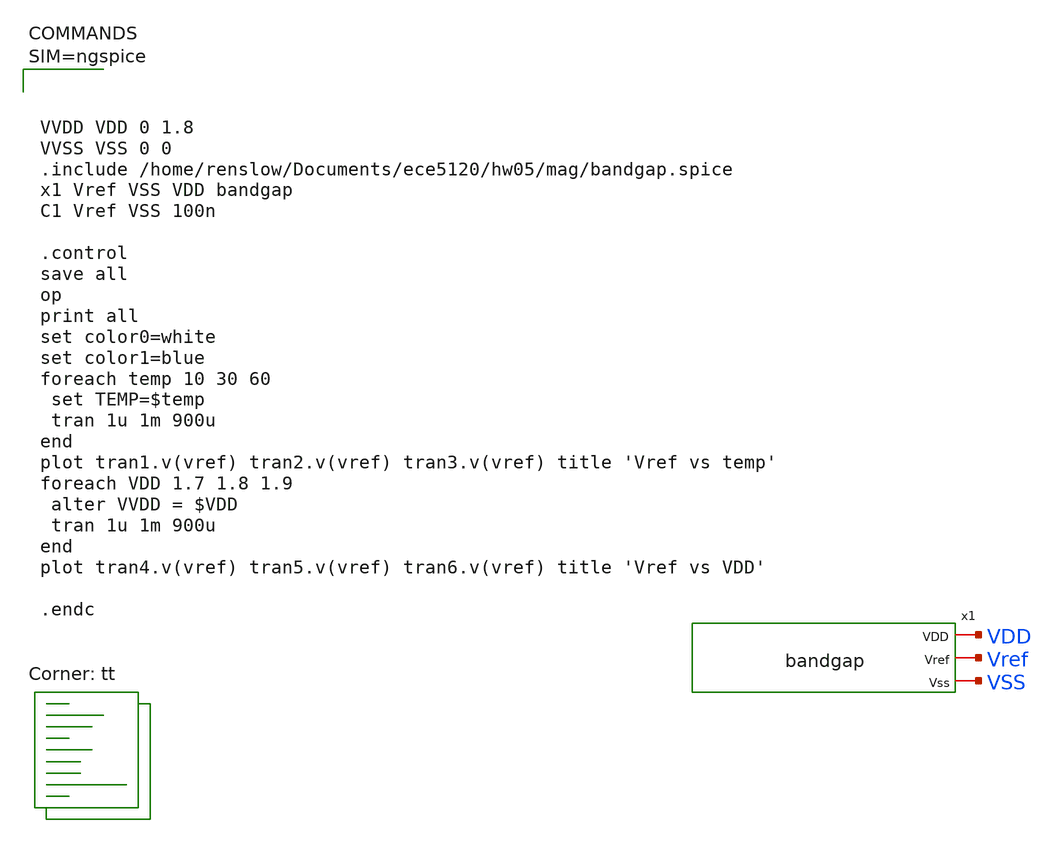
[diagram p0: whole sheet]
** sch_path: hw05/mag/bandgap_tb.sch
**.subckt bandgap_tb
x1 VDD Vref VSS bandgap
**** begin user architecture code
.lib $::SKYWATER_MODELS/sky130.lib.spice tt




VVDD VDD 0 1.8
VVSS VSS 0 0
.include /home/renslow/Documents/ece5120/hw05/mag/bandgap.spice
x1 Vref VSS VDD bandgap
C1 Vref VSS 100n

.control
save all
op
print all
set color0=white
set color1=blue
foreach temp 10 30 60
 set TEMP=$temp
 tran 1u 1m 900u
end
plot tran1.v(vref) tran2.v(vref) tran3.v(vref) title 'Vref vs temp'
foreach VDD 1.7 1.8 1.9
 alter VVDD = $VDD
 tran 1u 1m 900u
end
plot tran4.v(vref) tran5.v(vref) tran6.v(vref) title 'Vref vs VDD'

.endc



**** end user architecture code
**.ends
.end
